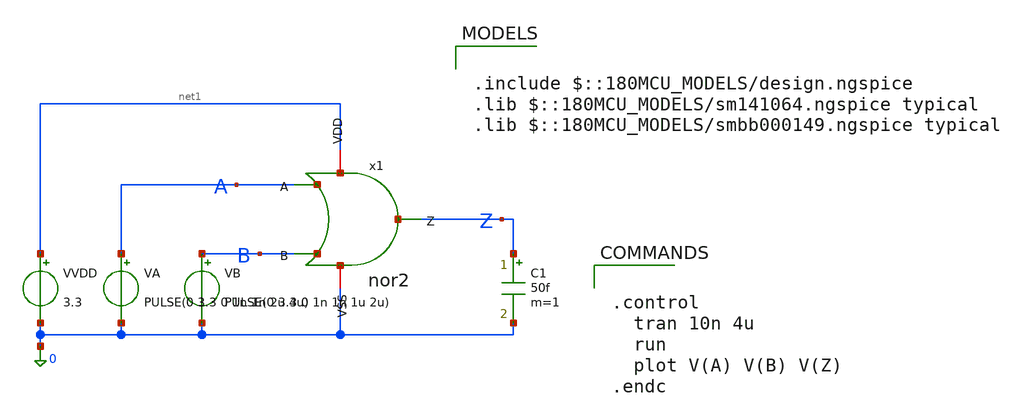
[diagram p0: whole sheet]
** sch_path: sar_logic/sar_designs/tb_nor2.sch
**.subckt tb_nor2
VB B 0 PULSE(0 3.3 0 1n 1n 1u 2u)
VA A 0 PULSE(0 3.3 0 1n 1n 2u 4u)
VVDD net1 0 3.3
C1 Z 0 50f m=1
x1 net1 A B Z 0 nor2
**** begin user architecture code

.include $::180MCU_MODELS/design.ngspice
.lib $::180MCU_MODELS/sm141064.ngspice typical
.lib $::180MCU_MODELS/smbb000149.ngspice typical



.control
  tran 10n 4u
  run
  plot V(A) V(B) V(Z)
.endc


**** end user architecture code
**.ends
.end
